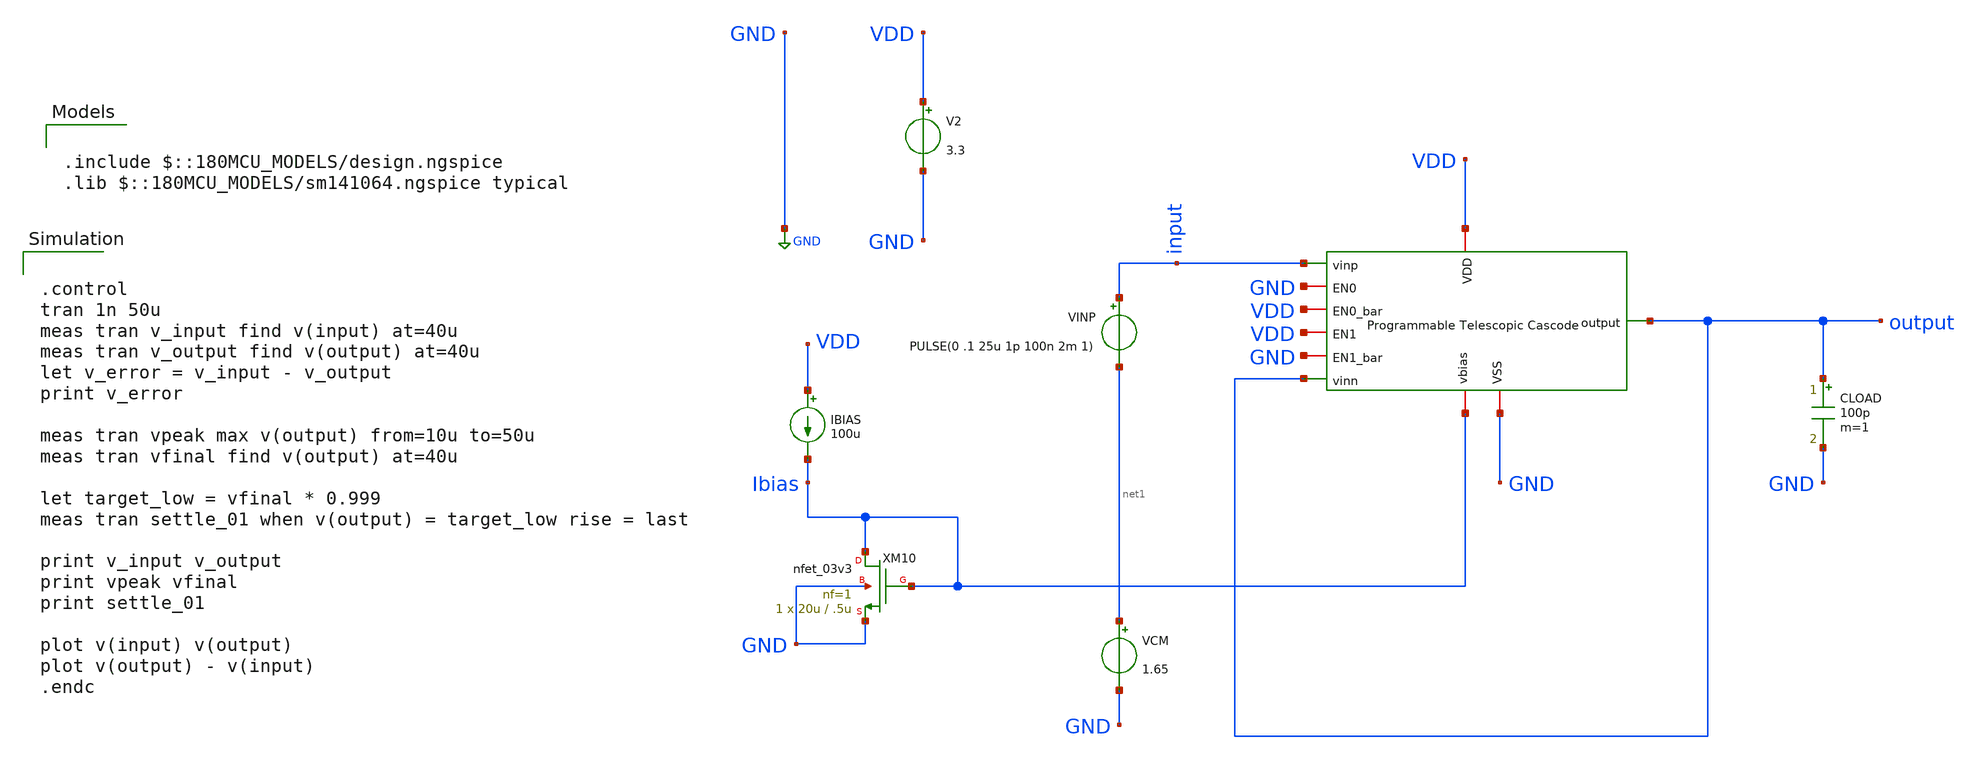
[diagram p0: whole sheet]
** sch_path: designs/libs/core_amps/ota_telescopic/programmable tb/programmable_telescopic_small_step_settling_tb.sch
**.subckt programmable_telescopic_small_step_settling_tb
V2 VDD GND 3.3
CLOAD output GND 100p m=1
VINP input net1 PULSE(0 .1 25u 1p 100n 2m 1)
VCM net1 GND 1.65
x1 VDD output GND VDD VDD GND output input GND Ibias programmable_telescopic_cascode
IBIAS VDD Ibias 100u
XM10 Ibias Ibias GND GND nfet_03v3 L=.5u W=20u nf=1 ad='int((nf+1)/2) * W/nf * 0.18u' as='int((nf+2)/2) * W/nf * 0.18u'
+ pd='2*int((nf+1)/2) * (W/nf + 0.18u)' ps='2*int((nf+2)/2) * (W/nf + 0.18u)' nrd='0.18u / W' nrs='0.18u / W'
+ sa=0 sb=0 sd=0 m=1
**** begin user architecture code

.include $::180MCU_MODELS/design.ngspice
.lib $::180MCU_MODELS/sm141064.ngspice typical



.control
tran 1n 50u
meas tran v_input find v(input) at=40u
meas tran v_output find v(output) at=40u
let v_error = v_input - v_output
print v_error

meas tran vpeak max v(output) from=10u to=50u
meas tran vfinal find v(output) at=40u

let target_low = vfinal * 0.999
meas tran settle_01 when v(output) = target_low rise = last

print v_input v_output
print vpeak vfinal
print settle_01

plot v(input) v(output)
plot v(output) - v(input)
.endc


**** end user architecture code
**.ends
.GLOBAL GND
.end
